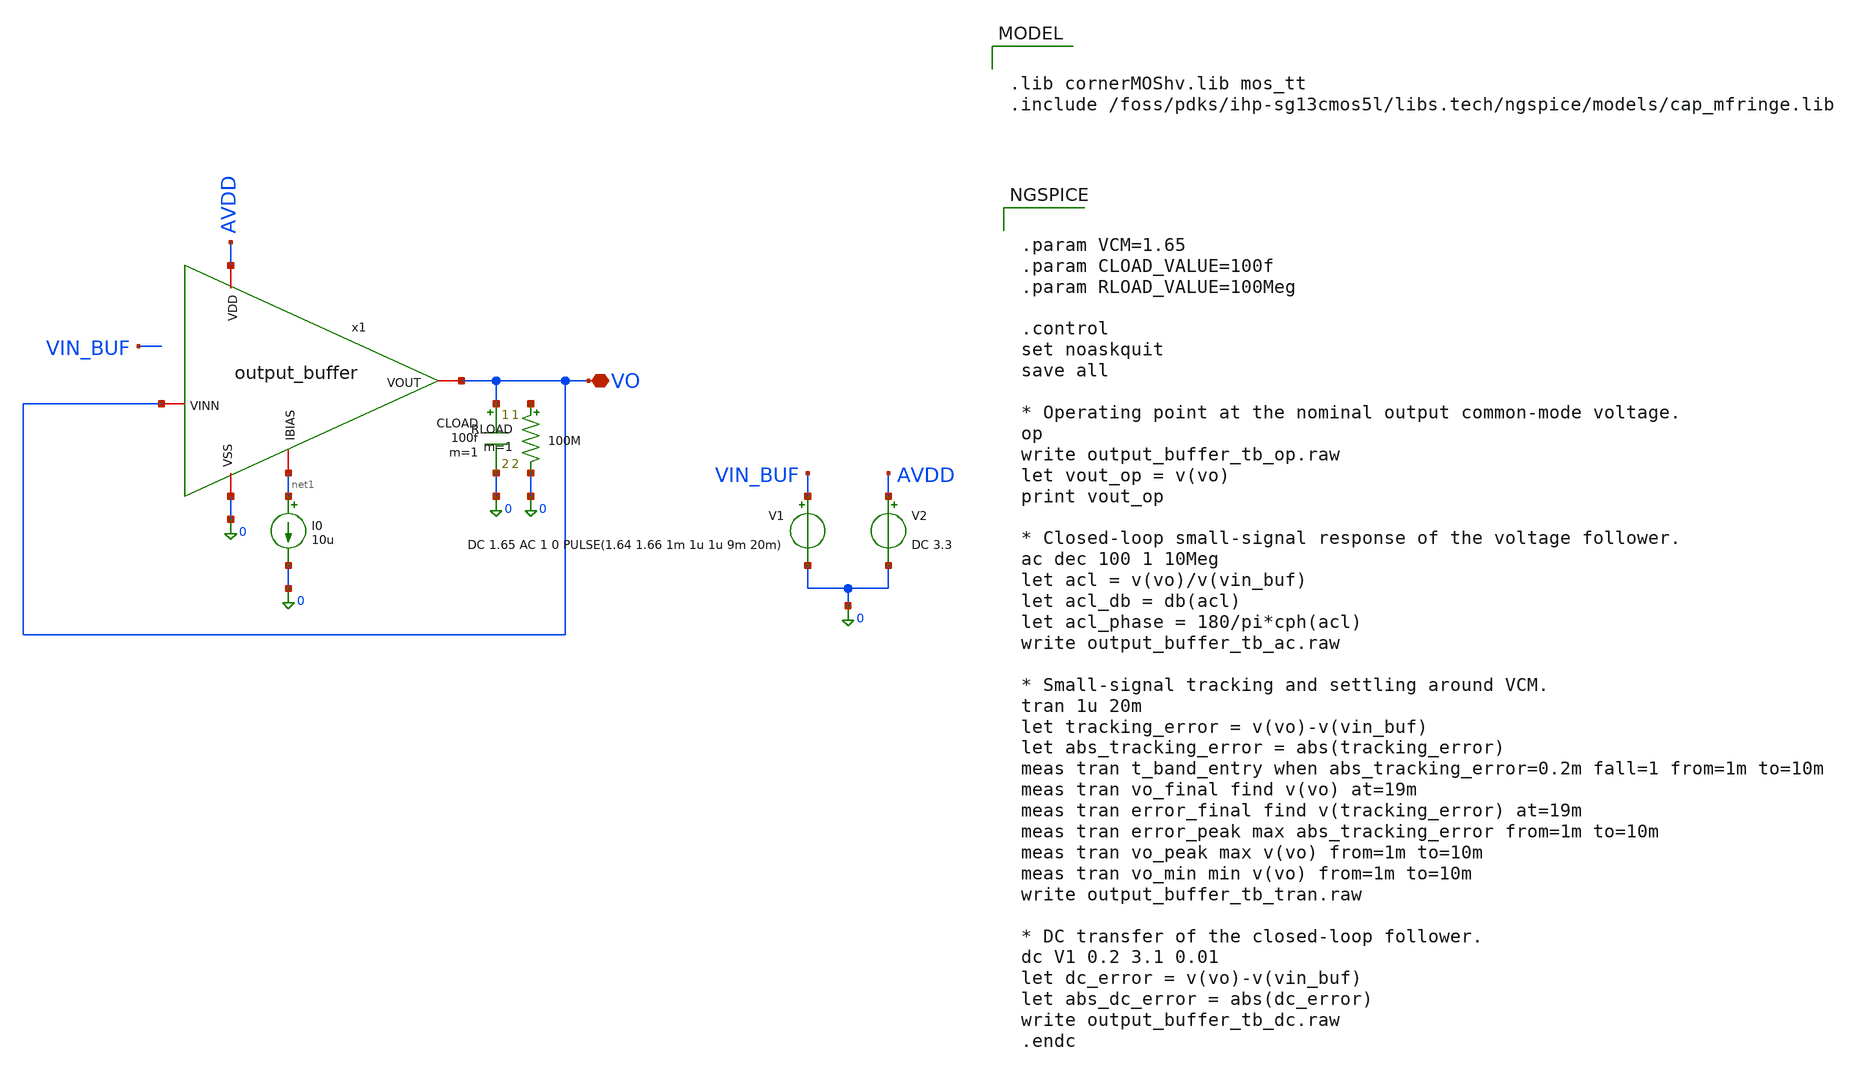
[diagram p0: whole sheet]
** sch_path: xschem/output_buffer/output_buffer_tb.sch
**.subckt output_buffer_tb VO
*.iopin VO
V1 VIN_BUF 0 DC 1.65 AC 1 0 PULSE(1.64 1.66 1m 1u 1u 9m 20m)
V2 AVDD 0 DC 3.3
CLOAD VO 0 100f m=1
I0 net1 0 10u
x1 AVDD 0 net1 VO VO output_buffer
RLOAD net2 0 100M m=1
**** begin user architecture code

.lib cornerMOShv.lib mos_tt
.include /foss/pdks/ihp-sg13cmos5l/libs.tech/ngspice/models/cap_mfringe.lib



.param VCM=1.65
.param CLOAD_VALUE=100f
.param RLOAD_VALUE=100Meg

.control
set noaskquit
save all

* Operating point at the nominal output common-mode voltage.
op
write output_buffer_tb_op.raw
let vout_op = v(vo)
print vout_op

* Closed-loop small-signal response of the voltage follower.
ac dec 100 1 10Meg
let acl = v(vo)/v(vin_buf)
let acl_db = db(acl)
let acl_phase = 180/pi*cph(acl)
write output_buffer_tb_ac.raw

* Small-signal tracking and settling around VCM.
tran 1u 20m
let tracking_error = v(vo)-v(vin_buf)
let abs_tracking_error = abs(tracking_error)
meas tran t_band_entry when abs_tracking_error=0.2m fall=1 from=1m to=10m
meas tran vo_final find v(vo) at=19m
meas tran error_final find v(tracking_error) at=19m
meas tran error_peak max abs_tracking_error from=1m to=10m
meas tran vo_peak max v(vo) from=1m to=10m
meas tran vo_min min v(vo) from=1m to=10m
write output_buffer_tb_tran.raw

* DC transfer of the closed-loop follower.
dc V1 0.2 3.1 0.01
let dc_error = v(vo)-v(vin_buf)
let abs_dc_error = abs(dc_error)
write output_buffer_tb_dc.raw
.endc


**** end user architecture code
**.ends

* expanding   symbol:
*+  /foss/designs/sg13cmos5l_spma_ip__instramp/xschem/output_buffer/output_buffer.sym # of pins=5
** sym_path: xschem/output_buffer/output_buffer.sym
** sch_path: xschem/output_buffer/output_buffer.sch
.subckt output_buffer VDD VSS IBIAS VINN VOUT
*.iopin VDD
*.iopin VSS
*.iopin IBIAS
*.iopin VINN
*.iopin VOUT
x1 VSS IBIAS VDD VINN VOUT VOUT ota_cmos5l
.ends


* expanding   symbol:  /foss/designs/sg13cmos5l_spma_ip__instramp/xschem/ota_cmos5l/ota_cmos5l.sym #
*+ of pins=6
** sym_path: xschem/output_buffer/ota_cmos5l.sym
** sch_path: xschem/output_buffer/ota_cmos5l.sch
.subckt ota_cmos5l VSS IBIAS VDD VINN VINP VOUT
*.iopin IBIAS
*.iopin VDD
*.iopin VSS
*.iopin VOUT
*.iopin VINP
*.iopin VINN
XM6 IBIAS IBIAS VDD VDD sg13_lv_pmos w={wbias} l={lbias} ng=1 m={m6} mm_ok=1
XM7 net1 IBIAS VDD VDD sg13_lv_pmos w={wbias} l={lbias} ng=1 m={m7} mm_ok=1
XM8 VOUT IBIAS VDD VDD sg13_lv_pmos w={wbias} l={lbias} ng=1 m={m8} mm_ok=1
XM1 net2 VINN net1 VDD sg13_lv_pmos w={winpair} l={linpair} ng=1 m=1 mm_ok=1
XM2 net3 VINP net1 VDD sg13_lv_pmos w={winpair} l={linpair} ng=1 m=1 mm_ok=1
XM3 net2 net2 VSS VSS sg13_lv_nmos w={wload} l={lload} ng=1 m=1 mm_ok=1
XM4 net3 net2 VSS VSS sg13_lv_nmos w={wload} l={lload} ng=1 m=1 mm_ok=1
XM5 VOUT net3 VSS VSS sg13_lv_nmos w={wcs} l={lcs} ng=1 m=1 mm_ok=1
XR1 net3 net4 VSS rhigh w=0.5e-6 l=1.95e-6 m=1 b=0 mm_ok=1
.save v(vinp)
.save v(vinn)
.save v(vout)
XC2 VOUT net4 cap_cmomi w=15e-6 l=15e-6 mmin=1 mmax=4 feed=double subblock=0 m=5 mm_ok=1
**** begin user architecture code


.param temp=27
.param lbias=0.15u wbias=0.15u
.param m6=1 m7=4 m8=8
.param linpair=3u winpair=20u
.param lload=5u wload=10u
.param lcs=3u wcs=20u
.param Cc=2p



**** end user architecture code
XC1 VOUT net4 cap_cmomi w=15e-6 l=15e-6 mmin=1 mmax=4 feed=double subblock=0 m=4 mm_ok=1
.ends

.end
